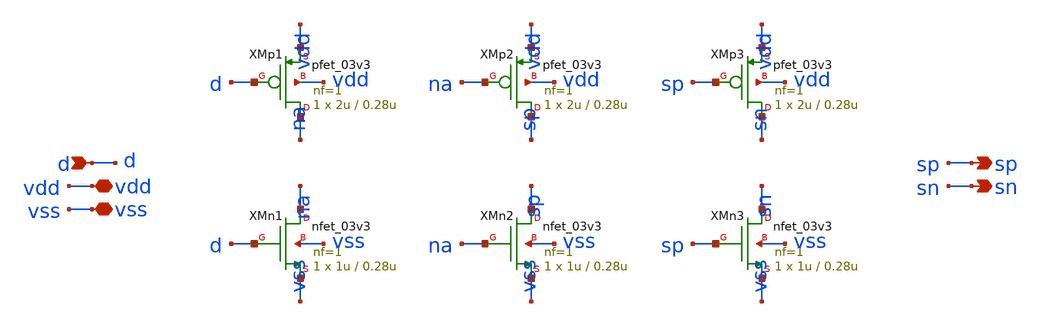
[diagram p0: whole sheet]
** sch_path: design/analog/driver.sch
**.subckt driver d vdd vss sp sn
*.ipin d
*.iopin vdd
*.iopin vss
*.opin sp
*.opin sn
XMp1 na d vdd vdd pfet_03v3 L=0.28u W=2u nf=1 ad='int((nf+1)/2) * W/nf * 0.18u' as='int((nf+2)/2) * W/nf * 0.18u'
+ pd='2*int((nf+1)/2) * (W/nf + 0.18u)' ps='2*int((nf+2)/2) * (W/nf + 0.18u)' nrd='0.18u / W' nrs='0.18u / W'
+ sa=0 sb=0 sd=0 m=1
XMn1 na d vss vss nfet_03v3 L=0.28u W=1u nf=1 ad='int((nf+1)/2) * W/nf * 0.18u' as='int((nf+2)/2) * W/nf * 0.18u'
+ pd='2*int((nf+1)/2) * (W/nf + 0.18u)' ps='2*int((nf+2)/2) * (W/nf + 0.18u)' nrd='0.18u / W' nrs='0.18u / W'
+ sa=0 sb=0 sd=0 m=1
XMp2 sp na vdd vdd pfet_03v3 L=0.28u W=2u nf=1 ad='int((nf+1)/2) * W/nf * 0.18u' as='int((nf+2)/2) * W/nf * 0.18u'
+ pd='2*int((nf+1)/2) * (W/nf + 0.18u)' ps='2*int((nf+2)/2) * (W/nf + 0.18u)' nrd='0.18u / W' nrs='0.18u / W'
+ sa=0 sb=0 sd=0 m=1
XMn2 sp na vss vss nfet_03v3 L=0.28u W=1u nf=1 ad='int((nf+1)/2) * W/nf * 0.18u' as='int((nf+2)/2) * W/nf * 0.18u'
+ pd='2*int((nf+1)/2) * (W/nf + 0.18u)' ps='2*int((nf+2)/2) * (W/nf + 0.18u)' nrd='0.18u / W' nrs='0.18u / W'
+ sa=0 sb=0 sd=0 m=1
XMp3 sn sp vdd vdd pfet_03v3 L=0.28u W=2u nf=1 ad='int((nf+1)/2) * W/nf * 0.18u' as='int((nf+2)/2) * W/nf * 0.18u'
+ pd='2*int((nf+1)/2) * (W/nf + 0.18u)' ps='2*int((nf+2)/2) * (W/nf + 0.18u)' nrd='0.18u / W' nrs='0.18u / W'
+ sa=0 sb=0 sd=0 m=1
XMn3 sn sp vss vss nfet_03v3 L=0.28u W=1u nf=1 ad='int((nf+1)/2) * W/nf * 0.18u' as='int((nf+2)/2) * W/nf * 0.18u'
+ pd='2*int((nf+1)/2) * (W/nf + 0.18u)' ps='2*int((nf+2)/2) * (W/nf + 0.18u)' nrd='0.18u / W' nrs='0.18u / W'
+ sa=0 sb=0 sd=0 m=1
**.ends
.end
